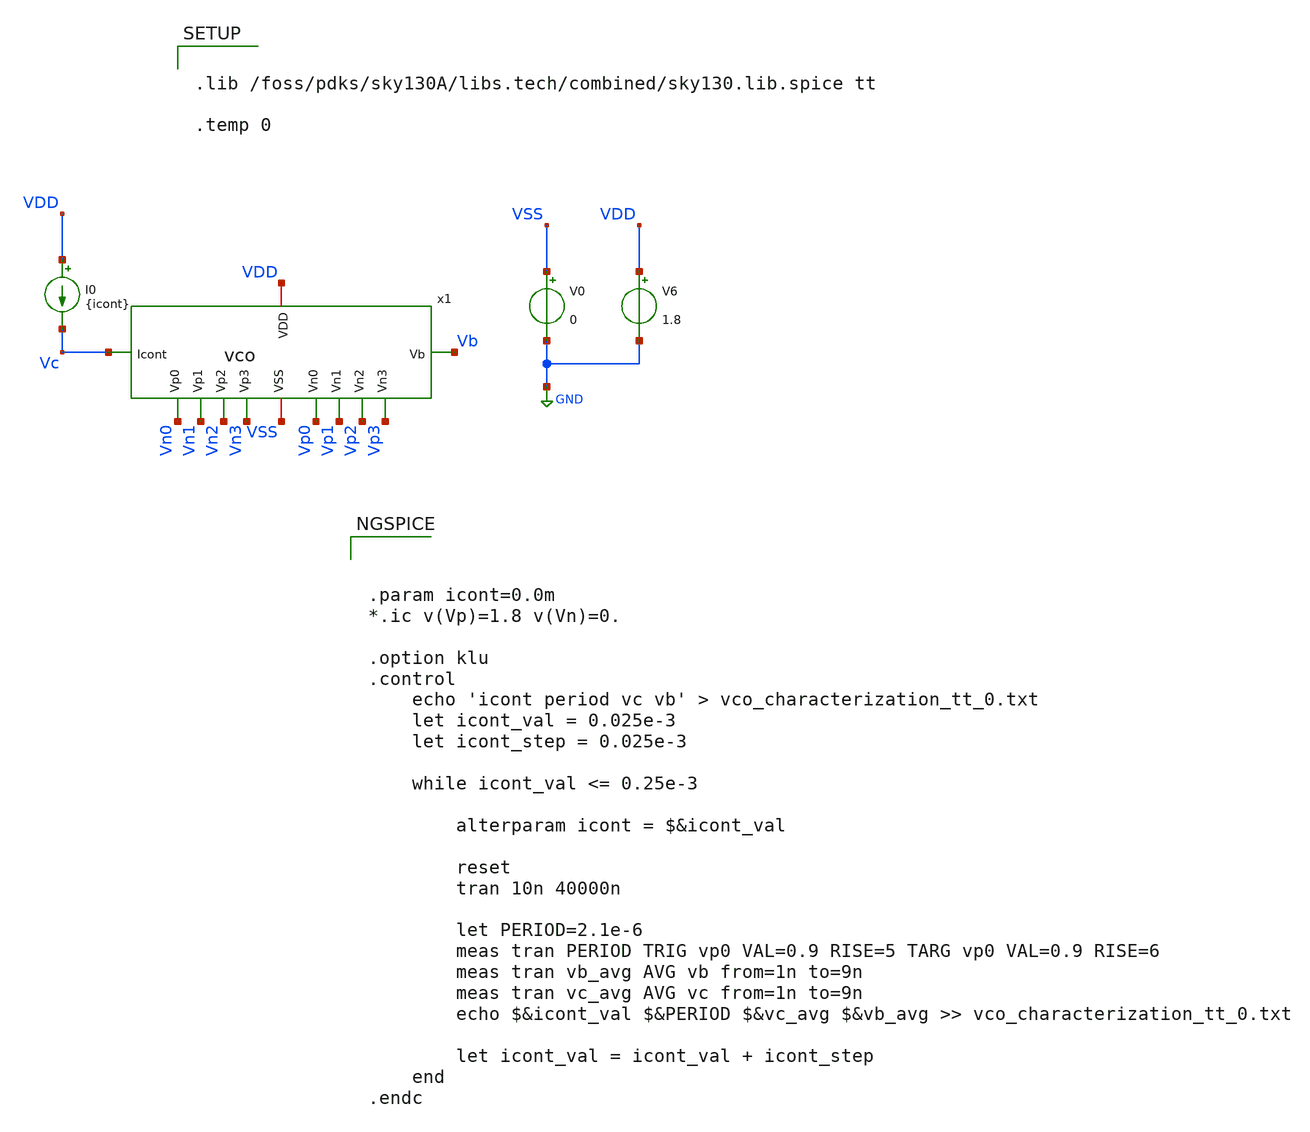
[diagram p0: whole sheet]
** sch_path: xschem/vco_characterization_tb.sch
**.subckt vco_characterization_tb
V0 VSS GND 0
V6 VDD GND 1.8
I0 VDD Vc {icont}
x1 VDD VSS Vc Vn0 Vn1 Vn2 Vn3 Vp0 Vp1 Vp2 Vp3 Vb vco
**** begin user architecture code



.param icont=0.0m
*.ic v(Vp)=1.8 v(Vn)=0.

.option klu
.control
	echo 'icont period vc vb' > vco_characterization_tt_0.txt
	let icont_val = 0.025e-3
	let icont_step = 0.025e-3

	while icont_val <= 0.25e-3

		alterparam icont = $&icont_val

		reset
		tran 10n 40000n

		let PERIOD=2.1e-6
		meas tran PERIOD TRIG vp0 VAL=0.9 RISE=5 TARG vp0 VAL=0.9 RISE=6
		meas tran vb_avg AVG vb from=1n to=9n
		meas tran vc_avg AVG vc from=1n to=9n
		echo $&icont_val $&PERIOD $&vc_avg $&vb_avg >> vco_characterization_tt_0.txt

		let icont_val = icont_val + icont_step
	end
.endc




.lib /foss/pdks/sky130A/libs.tech/combined/sky130.lib.spice tt

.temp 0


**** end user architecture code
**.ends

* expanding   symbol:  vco.sym # of pins=12
** sym_path: xschem-pex/vco.sym
.include ./vco.spice
.GLOBAL GND
.end
